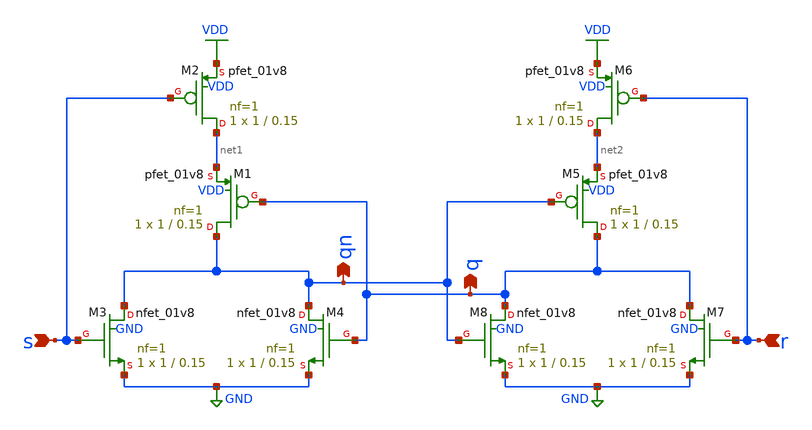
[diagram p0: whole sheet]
** sch_path: xschem/sr_latch.sch
**.subckt sr_latch s r qn q
*.ipin s
*.ipin r
*.opin qn
*.opin q
XM1 qn q net1 VDD sky130_fd_pr__pfet_01v8 L=0.15 W=1 nf=1 ad='int((1 + 1)/2) * 1 / 1 * 0.29' as='int((1 + 2)/2) * 1 / 1 * 0.29'
+ pd='2*int((1 + 1)/2) * (1 / 1 + 0.29)' ps='2*int((1 + 2)/2) * (1 / 1 + 0.29)' nrd='0.29 / 1 ' nrs='0.29 / 1 '
+ sa=0 sb=0 sd=0 mult=1 m=1
XM2 net1 s VDD VDD sky130_fd_pr__pfet_01v8 L=0.15 W=1 nf=1 ad='int((1 + 1)/2) * 1 / 1 * 0.29' as='int((1 + 2)/2) * 1 / 1 * 0.29'
+ pd='2*int((1 + 1)/2) * (1 / 1 + 0.29)' ps='2*int((1 + 2)/2) * (1 / 1 + 0.29)' nrd='0.29 / 1 ' nrs='0.29 / 1 '
+ sa=0 sb=0 sd=0 mult=1 m=1
XM3 qn s GND GND sky130_fd_pr__nfet_01v8 L=0.15 W=1 nf=1 ad='int((1 + 1)/2) * 1 / 1 * 0.29' as='int((1 + 2)/2) * 1 / 1 * 0.29'
+ pd='2*int((1 + 1)/2) * (1 / 1 + 0.29)' ps='2*int((1 + 2)/2) * (1 / 1 + 0.29)' nrd='0.29 / 1 ' nrs='0.29 / 1 '
+ sa=0 sb=0 sd=0 mult=1 m=1
XM4 qn q GND GND sky130_fd_pr__nfet_01v8 L=0.15 W=1 nf=1 ad='int((1 + 1)/2) * 1 / 1 * 0.29' as='int((1 + 2)/2) * 1 / 1 * 0.29'
+ pd='2*int((1 + 1)/2) * (1 / 1 + 0.29)' ps='2*int((1 + 2)/2) * (1 / 1 + 0.29)' nrd='0.29 / 1 ' nrs='0.29 / 1 '
+ sa=0 sb=0 sd=0 mult=1 m=1
XM5 q qn net2 VDD sky130_fd_pr__pfet_01v8 L=0.15 W=1 nf=1 ad='int((1 + 1)/2) * 1 / 1 * 0.29' as='int((1 + 2)/2) * 1 / 1 * 0.29'
+ pd='2*int((1 + 1)/2) * (1 / 1 + 0.29)' ps='2*int((1 + 2)/2) * (1 / 1 + 0.29)' nrd='0.29 / 1 ' nrs='0.29 / 1 '
+ sa=0 sb=0 sd=0 mult=1 m=1
XM6 net2 r VDD VDD sky130_fd_pr__pfet_01v8 L=0.15 W=1 nf=1 ad='int((1 + 1)/2) * 1 / 1 * 0.29' as='int((1 + 2)/2) * 1 / 1 * 0.29'
+ pd='2*int((1 + 1)/2) * (1 / 1 + 0.29)' ps='2*int((1 + 2)/2) * (1 / 1 + 0.29)' nrd='0.29 / 1 ' nrs='0.29 / 1 '
+ sa=0 sb=0 sd=0 mult=1 m=1
XM7 q r GND GND sky130_fd_pr__nfet_01v8 L=0.15 W=1 nf=1 ad='int((1 + 1)/2) * 1 / 1 * 0.29' as='int((1 + 2)/2) * 1 / 1 * 0.29'
+ pd='2*int((1 + 1)/2) * (1 / 1 + 0.29)' ps='2*int((1 + 2)/2) * (1 / 1 + 0.29)' nrd='0.29 / 1 ' nrs='0.29 / 1 '
+ sa=0 sb=0 sd=0 mult=1 m=1
XM8 q qn GND GND sky130_fd_pr__nfet_01v8 L=0.15 W=1 nf=1 ad='int((1 + 1)/2) * 1 / 1 * 0.29' as='int((1 + 2)/2) * 1 / 1 * 0.29'
+ pd='2*int((1 + 1)/2) * (1 / 1 + 0.29)' ps='2*int((1 + 2)/2) * (1 / 1 + 0.29)' nrd='0.29 / 1 ' nrs='0.29 / 1 '
+ sa=0 sb=0 sd=0 mult=1 m=1
**.ends
.GLOBAL VDD
.GLOBAL GND
.end
